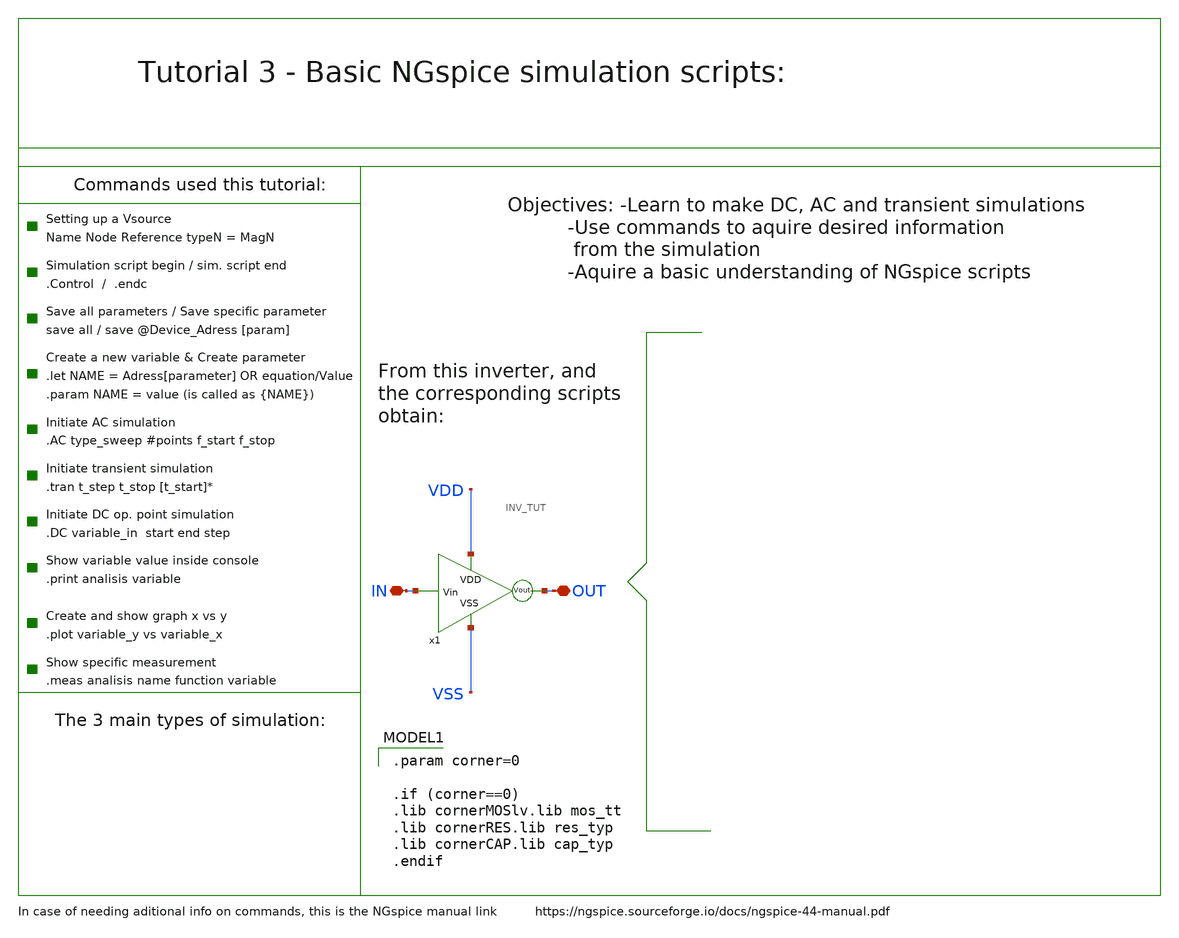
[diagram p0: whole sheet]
** sch_path: Tutoriales/Tutorial_3.sch
**.subckt Tutorial_3 IN OUT
*.iopin IN
*.iopin OUT
x1 VSS VDD OUT IN INV_TUT
**** begin user architecture code



vvdd vdd 0 dc 1.8
vvss vss 0 0
VINN IN 0 dc 0.2
cload OUT 0 5p

.control
save all
DC VINN 0.2 1.8 0.2
plot v(OUT) vs v(IN)
meas dc Average AVG v(OUT)
meas dc RMS RMS v(OUT)
meas dc INT INTEG v(OUT)
.endc


.end


 .param corner=0

.if (corner==0)
.lib cornerMOSlv.lib mos_tt
.lib cornerRES.lib res_typ
.lib cornerCAP.lib cap_typ
.endif

**** end user architecture code
**.ends

* expanding   symbol:  /foss/designs/Tutoriales_Xschem/Tutoriales/INV_TUT.sym # of pins=4
** sym_path: Tutoriales/INV_TUT.sym
** sch_path: Tutoriales/INV_TUT.sch
.subckt INV_TUT VSS VDD Vout Vin
*.ipin Vin
*.opin Vout
*.ipin VSS
*.ipin VDD
XM1 Vout Vin VSS net1 sg13_lv_nmos w=0.15u l=0.13u ng=1 m=1 mm_ok=1
XM2 Vout Vin VDD net2 sg13_lv_pmos w=0.45u l=0.13u ng=1 m=1 mm_ok=1
.ends

.end
